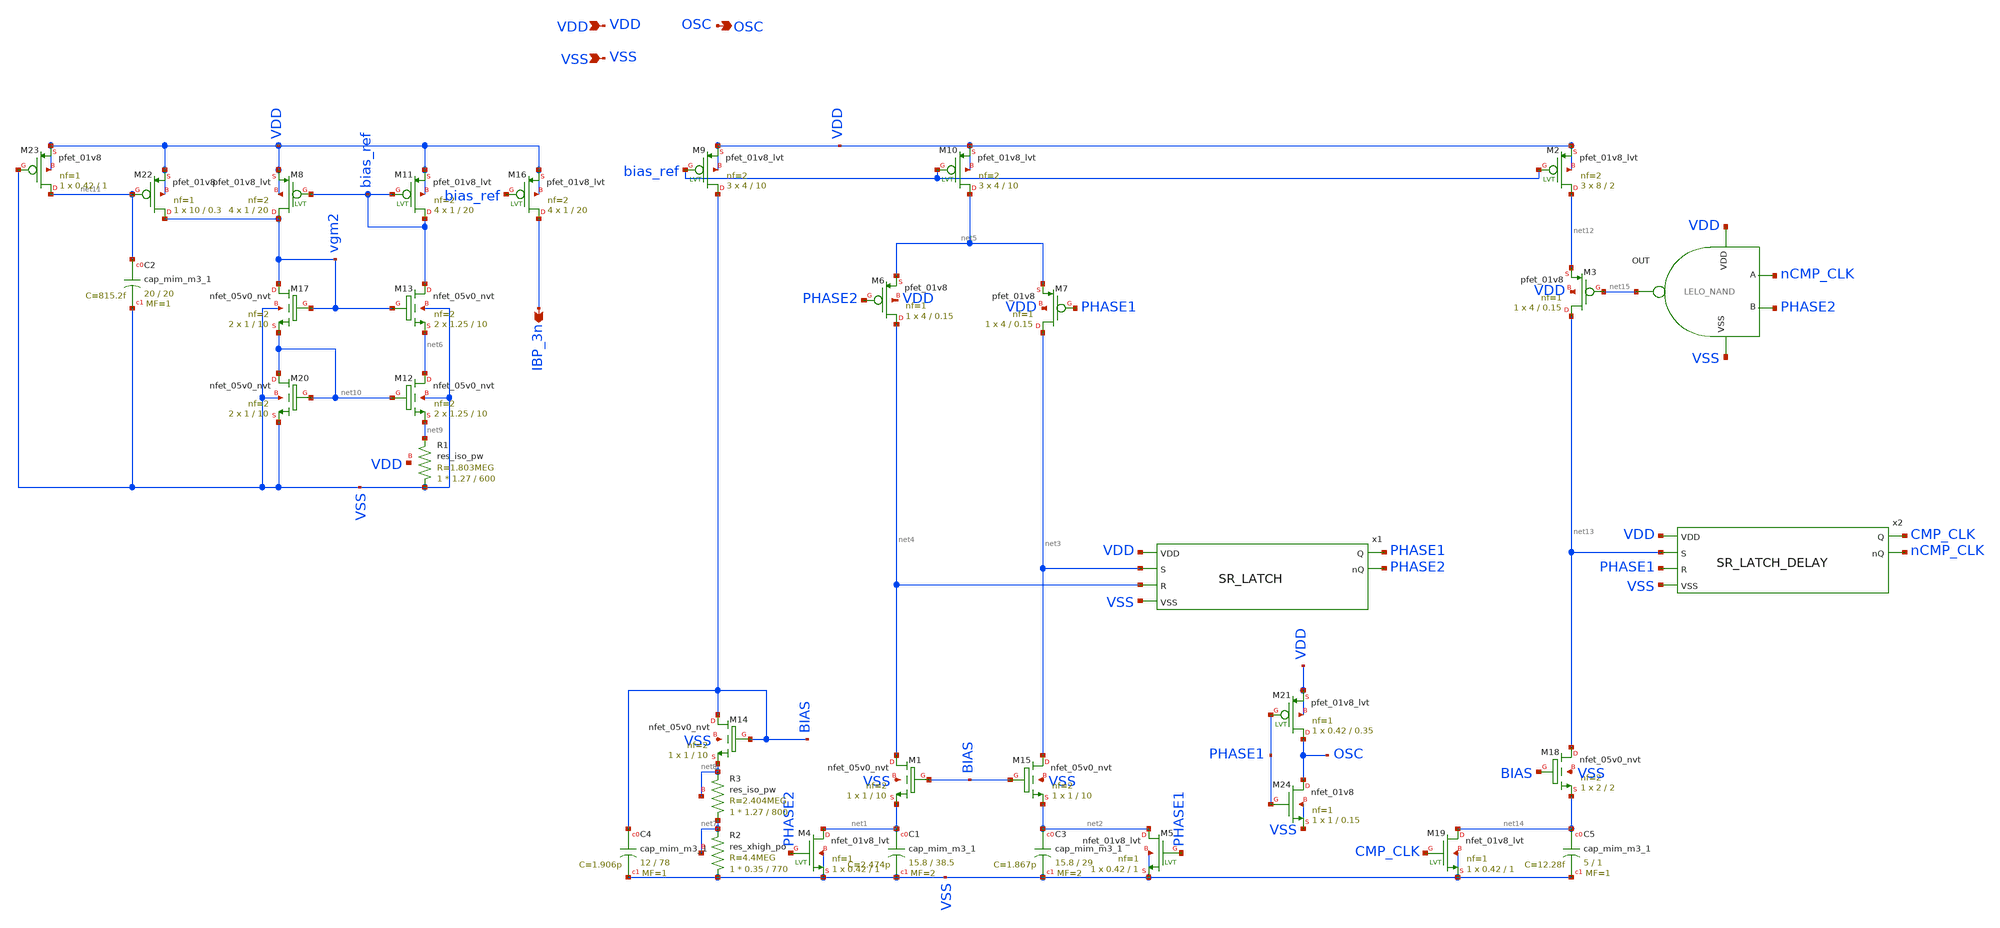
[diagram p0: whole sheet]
** sch_path: design/LELO_SVOD_SKY130A/LELO_SVOD_RELOSC.sch
**.subckt LELO_SVOD_RELOSC VDD VSS OSC IBP_3n
*.ipin VDD
*.ipin VSS
*.opin OSC
*.opin IBP_3n
XM11 bias_ref bias_ref VDD VDD sky130_fd_pr__pfet_01v8_lvt L=20 W=1 nf=2 ad='int((2 + 1)/2) * 1 / 2 * 0.29'
+ as='int((2 + 2)/2) * 1 / 2 * 0.29' pd='2*int((2 + 1)/2) * (1 / 2 + 0.29)' ps='2*int((2 + 2)/2) * (1 / 2 + 0.29)'
+ nrd='0.29 / 1 ' nrs='0.29 / 1 ' sa=0 sb=0 sd=0 mult=4 m=4
XC3 net2 VSS sky130_fd_pr__cap_mim_m3_1 W=15.8 L=29 MF=2 m=2
XC1 net1 VSS sky130_fd_pr__cap_mim_m3_1 W=15.8 L=38.5 MF=2 m=2
XM8 vgm2 bias_ref VDD VDD sky130_fd_pr__pfet_01v8_lvt L=20 W=1 nf=2 ad='int((2 + 1)/2) * 1 / 2 * 0.29'
+ as='int((2 + 2)/2) * 1 / 2 * 0.29' pd='2*int((2 + 1)/2) * (1 / 2 + 0.29)' ps='2*int((2 + 2)/2) * (1 / 2 + 0.29)'
+ nrd='0.29 / 1 ' nrs='0.29 / 1 ' sa=0 sb=0 sd=0 mult=4 m=4
XM9 BIAS bias_ref VDD VDD sky130_fd_pr__pfet_01v8_lvt L=10 W=4 nf=2 ad='int((2 + 1)/2) * 4 / 2 * 0.29'
+ as='int((2 + 2)/2) * 4 / 2 * 0.29' pd='2*int((2 + 1)/2) * (4 / 2 + 0.29)' ps='2*int((2 + 2)/2) * (4 / 2 + 0.29)'
+ nrd='0.29 / 4 ' nrs='0.29 / 4 ' sa=0 sb=0 sd=0 mult=3 m=3
XM10 net5 bias_ref VDD VDD sky130_fd_pr__pfet_01v8_lvt L=10 W=4 nf=2 ad='int((2 + 1)/2) * 4 / 2 * 0.29'
+ as='int((2 + 2)/2) * 4 / 2 * 0.29' pd='2*int((2 + 1)/2) * (4 / 2 + 0.29)' ps='2*int((2 + 2)/2) * (4 / 2 + 0.29)'
+ nrd='0.29 / 4 ' nrs='0.29 / 4 ' sa=0 sb=0 sd=0 mult=3 m=3
XM24 OSC PHASE1 VSS VSS sky130_fd_pr__nfet_01v8 L=0.15 W=1 nf=1 ad='int((1 + 1)/2) * 1 / 1 * 0.29' as='int((1 + 2)/2) * 1 / 1 * 0.29'
+ pd='2*int((1 + 1)/2) * (1 / 1 + 0.29)' ps='2*int((1 + 2)/2) * (1 / 1 + 0.29)' nrd='0.29 / 1 ' nrs='0.29 / 1 '
+ sa=0 sb=0 sd=0 mult=1 m=1
XC4 BIAS VSS sky130_fd_pr__cap_mim_m3_1 W=12 L=78 MF=1 m=1
XM1 net4 BIAS net1 VSS sky130_fd_pr__nfet_05v0_nvt L=10 W=1 nf=2 ad='int((2 + 1)/2) * 1 / 2 * 0.29' as='int((2 + 2)/2) * 1 / 2 * 0.29'
+ pd='2*int((2 + 1)/2) * (1 / 2 + 0.29)' ps='2*int((2 + 2)/2) * (1 / 2 + 0.29)' nrd='0.29 / 1 ' nrs='0.29 / 1 '
+ sa=0 sb=0 sd=0 mult=1 m=1
XM14 BIAS BIAS net8 VSS sky130_fd_pr__nfet_05v0_nvt L=10 W=1 nf=2 ad='int((2 + 1)/2) * 1 / 2 * 0.29'
+ as='int((2 + 2)/2) * 1 / 2 * 0.29' pd='2*int((2 + 1)/2) * (1 / 2 + 0.29)' ps='2*int((2 + 2)/2) * (1 / 2 + 0.29)'
+ nrd='0.29 / 1 ' nrs='0.29 / 1 ' sa=0 sb=0 sd=0 mult=1 m=1
XM15 net3 BIAS net2 VSS sky130_fd_pr__nfet_05v0_nvt L=10 W=1 nf=2 ad='int((2 + 1)/2) * 1 / 2 * 0.29'
+ as='int((2 + 2)/2) * 1 / 2 * 0.29' pd='2*int((2 + 1)/2) * (1 / 2 + 0.29)' ps='2*int((2 + 2)/2) * (1 / 2 + 0.29)'
+ nrd='0.29 / 1 ' nrs='0.29 / 1 ' sa=0 sb=0 sd=0 mult=1 m=1
XR3 net7 net8 net8 sky130_fd_pr__res_iso_pw W=1.27 L=800 m=1
XR2 VSS net7 net7 sky130_fd_pr__res_xhigh_po W=0.35 L=770 mult=1 m=1
XR1 VSS net9 VDD sky130_fd_pr__res_iso_pw W=1.27 L=600 m=1
XM13 bias_ref vgm2 net6 VSS sky130_fd_pr__nfet_05v0_nvt L=10 W=1.25 nf=2 ad='int((2 + 1)/2) * 1.25 / 2 * 0.29'
+ as='int((2 + 2)/2) * 1.25 / 2 * 0.29' pd='2*int((2 + 1)/2) * (1.25 / 2 + 0.29)' ps='2*int((2 + 2)/2) * (1.25 / 2 + 0.29)'
+ nrd='0.29 / 1.25 ' nrs='0.29 / 1.25 ' sa=0 sb=0 sd=0 mult=2 m=2
XM17 vgm2 vgm2 net10 VSS sky130_fd_pr__nfet_05v0_nvt L=10 W=1 nf=2 ad='int((2 + 1)/2) * 1 / 2 * 0.29'
+ as='int((2 + 2)/2) * 1 / 2 * 0.29' pd='2*int((2 + 1)/2) * (1 / 2 + 0.29)' ps='2*int((2 + 2)/2) * (1 / 2 + 0.29)'
+ nrd='0.29 / 1 ' nrs='0.29 / 1 ' sa=0 sb=0 sd=0 mult=2 m=2
XM20 net10 net10 VSS VSS sky130_fd_pr__nfet_05v0_nvt L=10 W=1 nf=2 ad='int((2 + 1)/2) * 1 / 2 * 0.29'
+ as='int((2 + 2)/2) * 1 / 2 * 0.29' pd='2*int((2 + 1)/2) * (1 / 2 + 0.29)' ps='2*int((2 + 2)/2) * (1 / 2 + 0.29)'
+ nrd='0.29 / 1 ' nrs='0.29 / 1 ' sa=0 sb=0 sd=0 mult=2 m=2
XM21 OSC PHASE1 VDD VDD sky130_fd_pr__pfet_01v8_lvt L=0.35 W=0.42 nf=1 ad='int((1 + 1)/2) * 0.42 / 1 * 0.29'
+ as='int((1 + 2)/2) * 0.42 / 1 * 0.29' pd='2*int((1 + 1)/2) * (0.42 / 1 + 0.29)' ps='2*int((1 + 2)/2) * (0.42 / 1 + 0.29)'
+ nrd='0.29 / 0.42 ' nrs='0.29 / 0.42 ' sa=0 sb=0 sd=0 mult=1 m=1
XM12 net6 net10 net9 VSS sky130_fd_pr__nfet_05v0_nvt L=10 W=1.25 nf=2 ad='int((2 + 1)/2) * 1.25 / 2 * 0.29'
+ as='int((2 + 2)/2) * 1.25 / 2 * 0.29' pd='2*int((2 + 1)/2) * (1.25 / 2 + 0.29)' ps='2*int((2 + 2)/2) * (1.25 / 2 + 0.29)'
+ nrd='0.29 / 1.25 ' nrs='0.29 / 1.25 ' sa=0 sb=0 sd=0 mult=2 m=2
XM6 net4 PHASE2 net5 VDD sky130_fd_pr__pfet_01v8 L=0.15 W=4 nf=1 ad='int((1 + 1)/2) * 4 / 1 * 0.29' as='int((1 + 2)/2) * 4 / 1 * 0.29'
+ pd='2*int((1 + 1)/2) * (4 / 1 + 0.29)' ps='2*int((1 + 2)/2) * (4 / 1 + 0.29)' nrd='0.29 / 4 ' nrs='0.29 / 4 '
+ sa=0 sb=0 sd=0 mult=1 m=1
XM7 net3 PHASE1 net5 VDD sky130_fd_pr__pfet_01v8 L=0.15 W=4 nf=1 ad='int((1 + 1)/2) * 4 / 1 * 0.29' as='int((1 + 2)/2) * 4 / 1 * 0.29'
+ pd='2*int((1 + 1)/2) * (4 / 1 + 0.29)' ps='2*int((1 + 2)/2) * (4 / 1 + 0.29)' nrd='0.29 / 4 ' nrs='0.29 / 4 '
+ sa=0 sb=0 sd=0 mult=1 m=1
XM16 IBP_3n bias_ref VDD VDD sky130_fd_pr__pfet_01v8_lvt L=20 W=1 nf=2 ad='int((2 + 1)/2) * 1 / 2 * 0.29'
+ as='int((2 + 2)/2) * 1 / 2 * 0.29' pd='2*int((2 + 1)/2) * (1 / 2 + 0.29)' ps='2*int((2 + 2)/2) * (1 / 2 + 0.29)'
+ nrd='0.29 / 1 ' nrs='0.29 / 1 ' sa=0 sb=0 sd=0 mult=4 m=4
XM22 vgm2 net11 VDD VDD sky130_fd_pr__pfet_01v8 L=0.3 W=10 nf=1 ad='int((1 + 1)/2) * 10 / 1 * 0.29' as='int((1 + 2)/2) * 10 / 1 * 0.29'
+ pd='2*int((1 + 1)/2) * (10 / 1 + 0.29)' ps='2*int((1 + 2)/2) * (10 / 1 + 0.29)' nrd='0.29 / 10 ' nrs='0.29 / 10 '
+ sa=0 sb=0 sd=0 mult=1 m=1
XM23 net11 VSS VDD VDD sky130_fd_pr__pfet_01v8 L=1 W=0.42 nf=1 ad='int((1 + 1)/2) * 0.42 / 1 * 0.29'
+ as='int((1 + 2)/2) * 0.42 / 1 * 0.29' pd='2*int((1 + 1)/2) * (0.42 / 1 + 0.29)' ps='2*int((1 + 2)/2) * (0.42 / 1 + 0.29)'
+ nrd='0.29 / 0.42 ' nrs='0.29 / 0.42 ' sa=0 sb=0 sd=0 mult=1 m=1
XC2 net11 VSS sky130_fd_pr__cap_mim_m3_1 W=20 L=20 MF=1 m=1
XM4 net1 PHASE2 VSS VSS sky130_fd_pr__nfet_01v8_lvt L=1 W=0.42 nf=1 ad='int((1 + 1)/2) * 0.42 / 1 * 0.29'
+ as='int((1 + 2)/2) * 0.42 / 1 * 0.29' pd='2*int((1 + 1)/2) * (0.42 / 1 + 0.29)' ps='2*int((1 + 2)/2) * (0.42 / 1 + 0.29)'
+ nrd='0.29 / 0.42 ' nrs='0.29 / 0.42 ' sa=0 sb=0 sd=0 mult=1 m=1
XM5 net2 PHASE1 VSS VSS sky130_fd_pr__nfet_01v8_lvt L=1 W=0.42 nf=1 ad='int((1 + 1)/2) * 0.42 / 1 * 0.29'
+ as='int((1 + 2)/2) * 0.42 / 1 * 0.29' pd='2*int((1 + 1)/2) * (0.42 / 1 + 0.29)' ps='2*int((1 + 2)/2) * (0.42 / 1 + 0.29)'
+ nrd='0.29 / 0.42 ' nrs='0.29 / 0.42 ' sa=0 sb=0 sd=0 mult=1 m=1
x1 PHASE1 VDD PHASE2 net3 net4 VSS SR_LATCH
XM2 net12 bias_ref VDD VDD sky130_fd_pr__pfet_01v8_lvt L=2 W=8 nf=2 ad='int((2 + 1)/2) * 8 / 2 * 0.29'
+ as='int((2 + 2)/2) * 8 / 2 * 0.29' pd='2*int((2 + 1)/2) * (8 / 2 + 0.29)' ps='2*int((2 + 2)/2) * (8 / 2 + 0.29)'
+ nrd='0.29 / 8 ' nrs='0.29 / 8 ' sa=0 sb=0 sd=0 mult=3 m=3
XM3 net13 net15 net12 VDD sky130_fd_pr__pfet_01v8 L=0.15 W=4 nf=1 ad='int((1 + 1)/2) * 4 / 1 * 0.29'
+ as='int((1 + 2)/2) * 4 / 1 * 0.29' pd='2*int((1 + 1)/2) * (4 / 1 + 0.29)' ps='2*int((1 + 2)/2) * (4 / 1 + 0.29)'
+ nrd='0.29 / 4 ' nrs='0.29 / 4 ' sa=0 sb=0 sd=0 mult=1 m=1
XM18 net13 BIAS net14 VSS sky130_fd_pr__nfet_05v0_nvt L=2 W=2 nf=2 ad='int((2 + 1)/2) * 2 / 2 * 0.29'
+ as='int((2 + 2)/2) * 2 / 2 * 0.29' pd='2*int((2 + 1)/2) * (2 / 2 + 0.29)' ps='2*int((2 + 2)/2) * (2 / 2 + 0.29)'
+ nrd='0.29 / 2 ' nrs='0.29 / 2 ' sa=0 sb=0 sd=0 mult=1 m=1
XC5 net14 VSS sky130_fd_pr__cap_mim_m3_1 W=5 L=1 MF=1 m=1
XM19 net14 CMP_CLK VSS VSS sky130_fd_pr__nfet_01v8_lvt L=1 W=0.42 nf=1 ad='int((1 + 1)/2) * 0.42 / 1 * 0.29'
+ as='int((1 + 2)/2) * 0.42 / 1 * 0.29' pd='2*int((1 + 1)/2) * (0.42 / 1 + 0.29)' ps='2*int((1 + 2)/2) * (0.42 / 1 + 0.29)'
+ nrd='0.29 / 0.42 ' nrs='0.29 / 0.42 ' sa=0 sb=0 sd=0 mult=1 m=1
x3 VDD net15 nCMP_CLK PHASE2 VSS LELO_NAND
x2 CMP_CLK VDD nCMP_CLK net13 PHASE1 VSS SR_LATCH_DELAY
**.ends
.end
